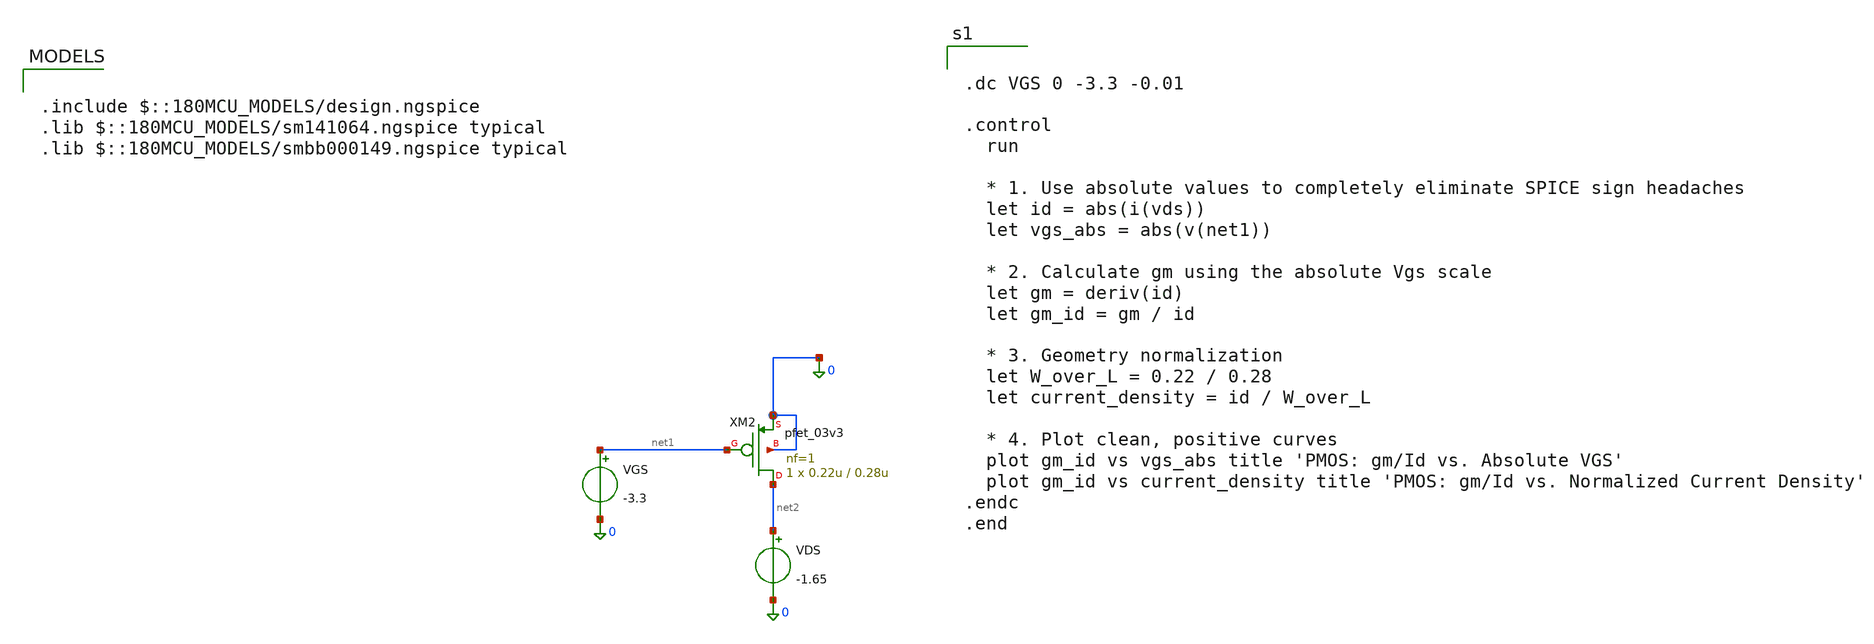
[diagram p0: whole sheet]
** sch_path: analog/blocks/Double_Tail_Comparator/pfet_test.sch
**.subckt pfet_test
VGS net1 0 -3.3
VDS net2 0 -1.65
XM2 net2 net1 0 0 pfet_03v3 L=0.28u W=0.22u nf=1 ad='int((nf+1)/2) * W/nf * 0.18u' as='int((nf+2)/2) * W/nf * 0.18u'
+ pd='2*int((nf+1)/2) * (W/nf + 0.18u)' ps='2*int((nf+2)/2) * (W/nf + 0.18u)' nrd='0.18u / W' nrs='0.18u / W'
+ sa=0 sb=0 sd=0 m=1
**** begin user architecture code

.include $::180MCU_MODELS/design.ngspice
.lib $::180MCU_MODELS/sm141064.ngspice typical
.lib $::180MCU_MODELS/smbb000149.ngspice typical



.dc VGS 0 -3.3 -0.01

.control
  run

  * 1. Use absolute values to completely eliminate SPICE sign headaches
  let id = abs(i(vds))
  let vgs_abs = abs(v(net1))

  * 2. Calculate gm using the absolute Vgs scale
  let gm = deriv(id)
  let gm_id = gm / id

  * 3. Geometry normalization
  let W_over_L = 0.22 / 0.28
  let current_density = id / W_over_L

  * 4. Plot clean, positive curves
  plot gm_id vs vgs_abs title 'PMOS: gm/Id vs. Absolute VGS'
  plot gm_id vs current_density title 'PMOS: gm/Id vs. Normalized Current Density'
.endc
.end


**** end user architecture code
**.ends
.end
